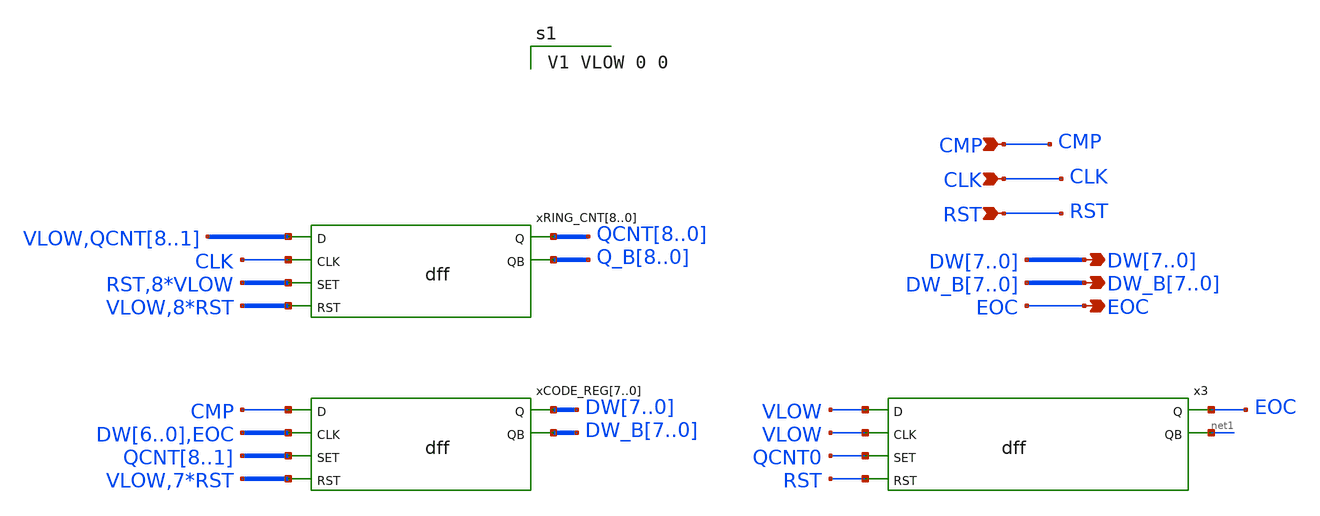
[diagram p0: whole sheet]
** sch_path: sar1.sch
**.subckt sar1 CMP CLK RST DW7,DW6,DW5,DW4,DW3,DW2,DW1,DW0
*+ DW_B7,DW_B6,DW_B5,DW_B4,DW_B3,DW_B2,DW_B1,DW_B0 EOC
*.ipin CMP
*.ipin CLK
*.ipin RST
*.opin DW7,DW6,DW5,DW4,DW3,DW2,DW1,DW0
*.opin DW_B7,DW_B6,DW_B5,DW_B4,DW_B3,DW_B2,DW_B1,DW_B0
*.opin EOC
xRING_CNT8 VLOW CLK QCNT8 RST Q_B8 VLOW dff
xRING_CNT7 QCNT8 CLK QCNT7 VLOW Q_B7 RST dff
xRING_CNT6 QCNT7 CLK QCNT6 VLOW Q_B6 RST dff
xRING_CNT5 QCNT6 CLK QCNT5 VLOW Q_B5 RST dff
xRING_CNT4 QCNT5 CLK QCNT4 VLOW Q_B4 RST dff
xRING_CNT3 QCNT4 CLK QCNT3 VLOW Q_B3 RST dff
xRING_CNT2 QCNT3 CLK QCNT2 VLOW Q_B2 RST dff
xRING_CNT1 QCNT2 CLK QCNT1 VLOW Q_B1 RST dff
xRING_CNT0 QCNT1 CLK QCNT0 VLOW Q_B0 RST dff
xCODE_REG7 CMP DW6 DW7 QCNT8 DW_B7 VLOW dff
xCODE_REG6 CMP DW5 DW6 QCNT7 DW_B6 RST dff
xCODE_REG5 CMP DW4 DW5 QCNT6 DW_B5 RST dff
xCODE_REG4 CMP DW3 DW4 QCNT5 DW_B4 RST dff
xCODE_REG3 CMP DW2 DW3 QCNT4 DW_B3 RST dff
xCODE_REG2 CMP DW1 DW2 QCNT3 DW_B2 RST dff
xCODE_REG1 CMP DW0 DW1 QCNT2 DW_B1 RST dff
xCODE_REG0 CMP EOC DW0 QCNT1 DW_B0 RST dff
x3 VLOW VLOW EOC QCNT0 net1 RST dff
**** begin user architecture code

V1 VLOW 0 0


**** end user architecture code
**.ends

* expanding   symbol:  dff.sym # of pins=6
** sym_path: dff.sym
** sch_path: dff.sch
.subckt dff D CLK Q SET QB RST
*.ipin D
*.ipin CLK
*.ipin SET
*.ipin RST
*.opin Q
*.opin QB
**** begin user architecture code

a1 D CLK SET RST Qi QBi flop1
.model flop1 d_dff(clk_delay = 1e-9 set_delay = 1e-9  reset_delay = 1e-9 ic = 2 rise_delay = 1e-9
+  fall_delay = 1e-9)

v1 Qi Q 0
V2 QBi QB 0


**** end user architecture code
.ends

.end
